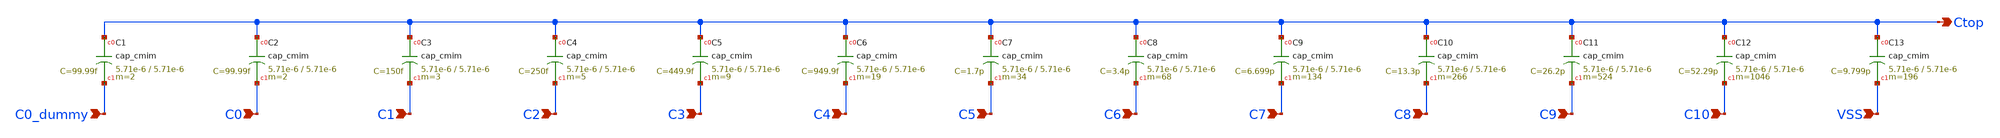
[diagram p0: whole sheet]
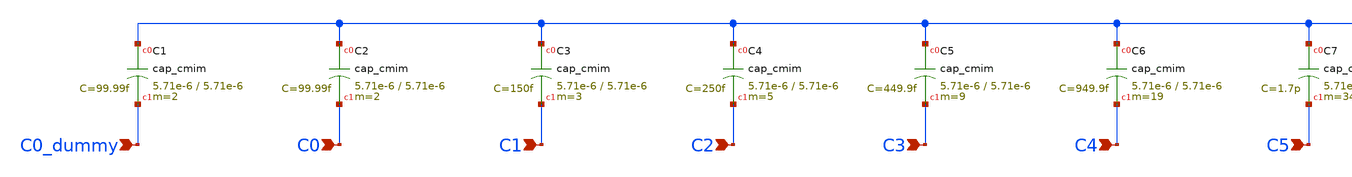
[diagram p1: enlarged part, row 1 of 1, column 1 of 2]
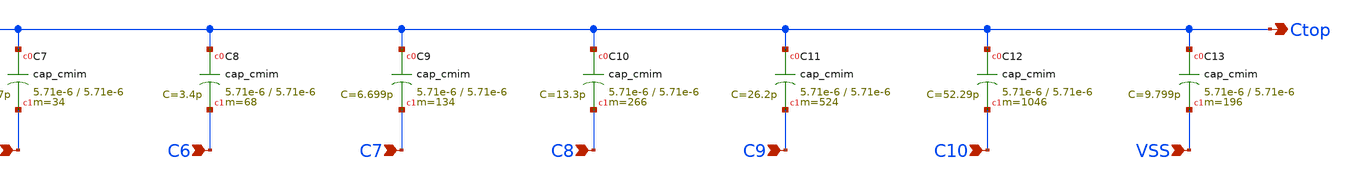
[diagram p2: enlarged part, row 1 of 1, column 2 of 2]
** sch_path: schematic/CDAC/CDAC.sch
**.subckt CDAC C0_dummy C0 C1 C2 C3 C4 C5 C6 C7 C8 C9 C10 VSS Ctop
*.ipin C0_dummy
*.ipin C0
*.ipin C1
*.ipin C2
*.ipin C3
*.ipin C4
*.ipin C5
*.ipin C6
*.ipin C7
*.ipin C8
*.ipin C9
*.ipin C10
*.ipin VSS
*.opin Ctop
XC1 Ctop C0_dummy cap_cmim w=5.71e-6 l=5.71e-6 m=2 mm_ok=1
XC2 Ctop C0 cap_cmim w=5.71e-6 l=5.71e-6 m=2 mm_ok=1
XC3 Ctop C1 cap_cmim w=5.71e-6 l=5.71e-6 m=3 mm_ok=1
XC4 Ctop C2 cap_cmim w=5.71e-6 l=5.71e-6 m=5 mm_ok=1
XC5 Ctop C3 cap_cmim w=5.71e-6 l=5.71e-6 m=9 mm_ok=1
XC6 Ctop C4 cap_cmim w=5.71e-6 l=5.71e-6 m=19 mm_ok=1
XC7 Ctop C5 cap_cmim w=5.71e-6 l=5.71e-6 m=34 mm_ok=1
XC8 Ctop C6 cap_cmim w=5.71e-6 l=5.71e-6 m=68 mm_ok=1
XC9 Ctop C7 cap_cmim w=5.71e-6 l=5.71e-6 m=134 mm_ok=1
XC10 Ctop C8 cap_cmim w=5.71e-6 l=5.71e-6 m=266 mm_ok=1
XC11 Ctop C9 cap_cmim w=5.71e-6 l=5.71e-6 m=524 mm_ok=1
XC12 Ctop C10 cap_cmim w=5.71e-6 l=5.71e-6 m=1046 mm_ok=1
XC13 Ctop VSS cap_cmim w=5.71e-6 l=5.71e-6 m=196 mm_ok=1
**.ends
.end
